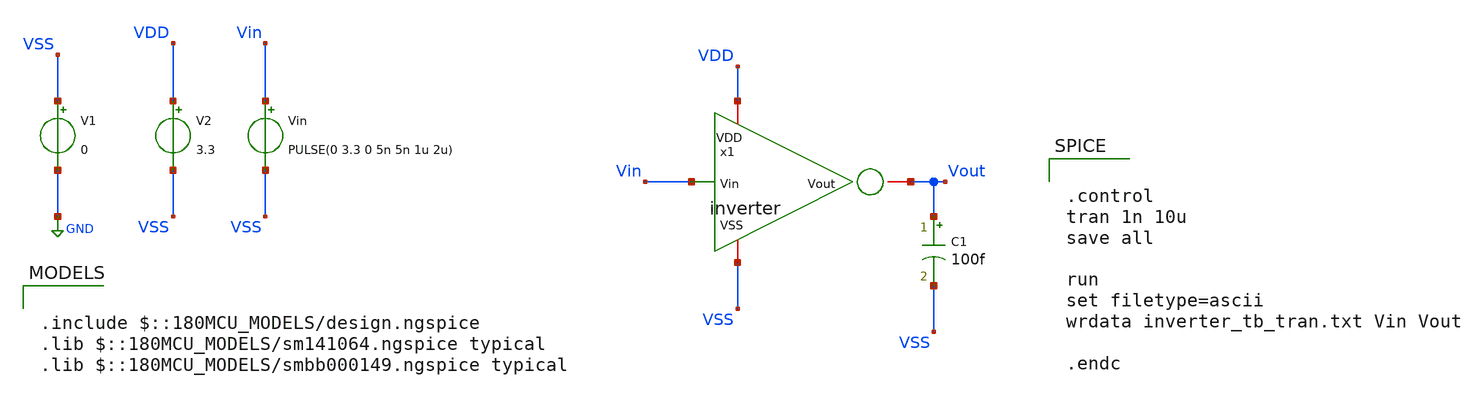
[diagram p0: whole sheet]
** sch_path: gf180_examples/inverter/xschem/inverter_tb_tran_colab.sch
**.subckt inverter_tb_tran_colab
x1 Vin VDD VSS Vout inverter
C1 Vout VSS 100f m=1
V1 VSS GND 0
V2 VDD VSS 3.3
Vin Vin VSS PULSE(0 3.3 0 5n 5n 1u 2u)
**** begin user architecture code

.include $::180MCU_MODELS/design.ngspice
.lib $::180MCU_MODELS/sm141064.ngspice typical
.lib $::180MCU_MODELS/smbb000149.ngspice typical



.control
tran 1n 10u
save all

run
set filetype=ascii
wrdata inverter_tb_tran.txt Vin Vout

.endc


**** end user architecture code
**.ends

* expanding   symbol:  inverter.sym # of pins=4
** sym_path: gf180_examples/inverter/xschem/inverter.sym
** sch_path: gf180_examples/inverter/xschem/inverter.sch
.subckt inverter Vin VDD VSS Vout
*.ipin Vin
*.iopin VDD
*.iopin VSS
*.iopin Vout
XM1 Vout Vin VSS VSS nfet_03v3 L=1u W=3u nf=1 ad='int((nf+1)/2) * W/nf * 0.18u' as='int((nf+2)/2) * W/nf * 0.18u'
+ pd='2*int((nf+1)/2) * (W/nf + 0.18u)' ps='2*int((nf+2)/2) * (W/nf + 0.18u)' nrd='0.18u / W' nrs='0.18u / W'
+ sa=0 sb=0 sd=0 m=1
XM2 Vout Vin VDD VDD pfet_03v3 L=1u W=3u nf=1 ad='int((nf+1)/2) * W/nf * 0.18u' as='int((nf+2)/2) * W/nf * 0.18u'
+ pd='2*int((nf+1)/2) * (W/nf + 0.18u)' ps='2*int((nf+2)/2) * (W/nf + 0.18u)' nrd='0.18u / W' nrs='0.18u / W'
+ sa=0 sb=0 sd=0 m=1
.ends

.GLOBAL GND
.end
